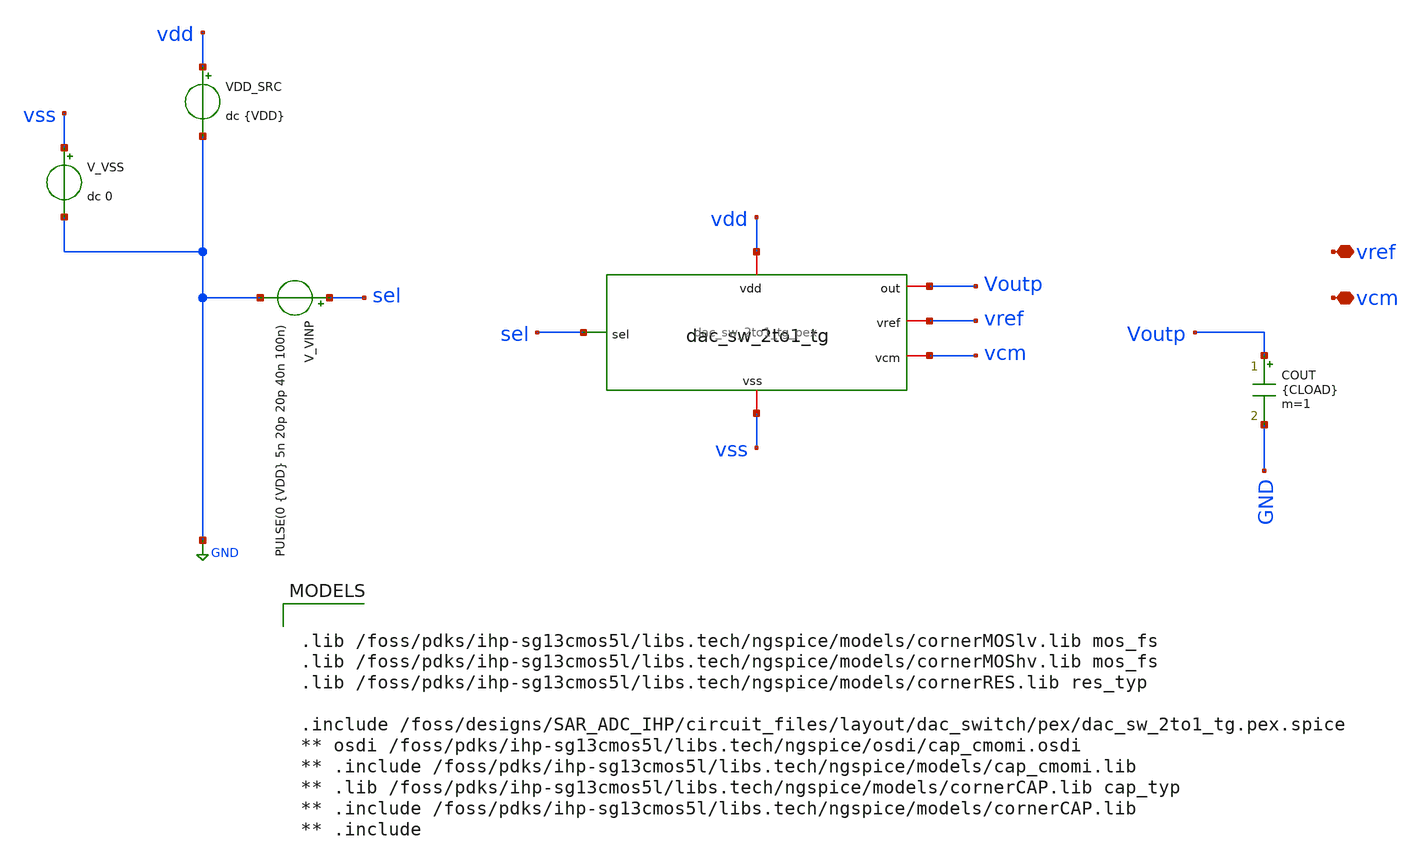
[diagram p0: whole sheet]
** sch_path: circuit_files/tb/dac_sw_tb_pex.sch
**.subckt dac_sw_tb_pex vref vcm
*.iopin vref
*.iopin vcm
VDD_SRC vdd GND dc {VDD}
V_VINP sel GND PULSE(0 {VDD} 5n 20p 20p 40n 100n)
V_VSS vss GND dc 0
COUT Voutp GND {CLOAD} m=1
x1 vss vref Voutp sel vcm vdd dac_sw_2to1_tg_pex
**** begin user architecture code

.lib /foss/pdks/ihp-sg13cmos5l/libs.tech/ngspice/models/cornerMOSlv.lib mos_fs
.lib /foss/pdks/ihp-sg13cmos5l/libs.tech/ngspice/models/cornerMOShv.lib mos_fs
.lib /foss/pdks/ihp-sg13cmos5l/libs.tech/ngspice/models/cornerRES.lib res_typ

.include /foss/designs/SAR_ADC_IHP/circuit_files/layout/dac_switch/pex/dac_sw_2to1_tg.pex.spice
** osdi /foss/pdks/ihp-sg13cmos5l/libs.tech/ngspice/osdi/cap_cmomi.osdi
** .include /foss/pdks/ihp-sg13cmos5l/libs.tech/ngspice/models/cap_cmomi.lib
** .lib /foss/pdks/ihp-sg13cmos5l/libs.tech/ngspice/models/cornerCAP.lib cap_typ
** .include /foss/pdks/ihp-sg13cmos5l/libs.tech/ngspice/models/cornerCAP.lib
** .include



* ============================================================
* Testbench parameters
* ============================================================

.param VDD   = 3.3
.param VCM   = 1.65
.param VREF  = 3.3
.param VDIFF = 0
.param CLOAD = 25.6p

* Local reference sources
VREF_SRC vref GND dc {VREF}
VVCM_SRC vcm  GND dc {VCM}

* Simulation options
.options savecurrents
.options reltol=1e-4
.options abstol=1e-12
.options vntol=1e-6
.options method=gear
.options maxord=2

* Save signals and currents
.save v(sel)
.save v(Voutp)
.save v(vref)
.save v(vcm)
.save v(vdd)
.save v(vss)
.save i(VDD_SRC)
.save i(VREF_SRC)
.save i(VVCM_SRC)

.control

shell rm -f dac_sw_results.txt

echo DAC switch PEX transient verification > dac_sw_results.txt
echo VDD = 3.3V >> dac_sw_results.txt
echo VCM = 1.65V >> dac_sw_results.txt
echo CLOAD = 25.6pF >> dac_sw_results.txt
echo Settling threshold = 5mV >> dac_sw_results.txt
echo columns: case out_low err_low out_high err_high out_return err_return pass >>
+ dac_sw_results.txt

* ============================================================
* CASE A: VREF = 3.3 V
* ============================================================

alterparam VREF = 3.3
reset
tran 2p 100n

write dac_sw_case_A.raw v(sel) v(Voutp) v(vref) v(vcm) v(vdd) v(vss) i(VDD_SRC) i(VREF_SRC)
+ i(VVCM_SRC)

meas tran out_low_A FIND v(Voutp) AT=4n
meas tran vcm_low_A FIND v(vcm) AT=4n
let err_low_A = out_low_A - vcm_low_A

meas tran out_high_A FIND v(Voutp) AT=20n
meas tran vref_high_A FIND v(vref) AT=20n
let err_high_A = out_high_A - vref_high_A

meas tran out_ret_A FIND v(Voutp) AT=80n
meas tran vcm_ret_A FIND v(vcm) AT=80n
let err_ret_A = out_ret_A - vcm_ret_A

let pass_low_A = 0
if abs(err_low_A) < 5m
  let pass_low_A = 1
end

let pass_high_A = 0
if abs(err_high_A) < 5m
  let pass_high_A = 1
end

let pass_return_A = 0
if abs(err_ret_A) < 5m
  let pass_return_A = 1
end

let pass_case_A = 0
if pass_low_A = 1
  if pass_high_A = 1
    if pass_return_A = 1
      let pass_case_A = 1
    end
  end
end

echo CASE_A $&out_low_A $&err_low_A $&out_high_A $&err_high_A $&out_ret_A $&err_ret_A $&pass_case_A
+ >> dac_sw_results.txt

* ============================================================
* CASE B: VREF = 0 V
* ============================================================

alterparam VREF = 0
reset
tran 2p 100n

write dac_sw_case_B.raw v(sel) v(Voutp) v(vref) v(vcm) v(vdd) v(vss) i(VDD_SRC) i(VREF_SRC)
+ i(VVCM_SRC)

meas tran out_low_B FIND v(Voutp) AT=4n
meas tran vcm_low_B FIND v(vcm) AT=4n
let err_low_B = out_low_B - vcm_low_B

meas tran out_high_B FIND v(Voutp) AT=20n
meas tran vref_high_B FIND v(vref) AT=20n
let err_high_B = out_high_B - vref_high_B

meas tran out_ret_B FIND v(Voutp) AT=80n
meas tran vcm_ret_B FIND v(vcm) AT=80n
let err_ret_B = out_ret_B - vcm_ret_B

let pass_low_B = 0
if abs(err_low_B) < 5m
  let pass_low_B = 1
end

let pass_high_B = 0
if abs(err_high_B) < 5m
  let pass_high_B = 1
end

let pass_return_B = 0
if abs(err_ret_B) < 5m
  let pass_return_B = 1
end

let pass_case_B = 0
if pass_low_B = 1
  if pass_high_B = 1
    if pass_return_B = 1
      let pass_case_B = 1
    end
  end
end

echo CASE_B $&out_low_B $&err_low_B $&out_high_B $&err_high_B $&out_ret_B $&err_ret_B $&pass_case_B
+ >> dac_sw_results.txt

* ============================================================
* Overall pass
* ============================================================

let pass_overall = 0
if pass_case_A = 1
  if pass_case_B = 1
    let pass_overall = 1
  end
end

echo pass_case_A = $&pass_case_A >> dac_sw_results.txt
echo pass_case_B = $&pass_case_B >> dac_sw_results.txt
echo pass_overall = $&pass_overall >> dac_sw_results.txt

.endc




**** end user architecture code
**.ends
.GLOBAL GND
.end
